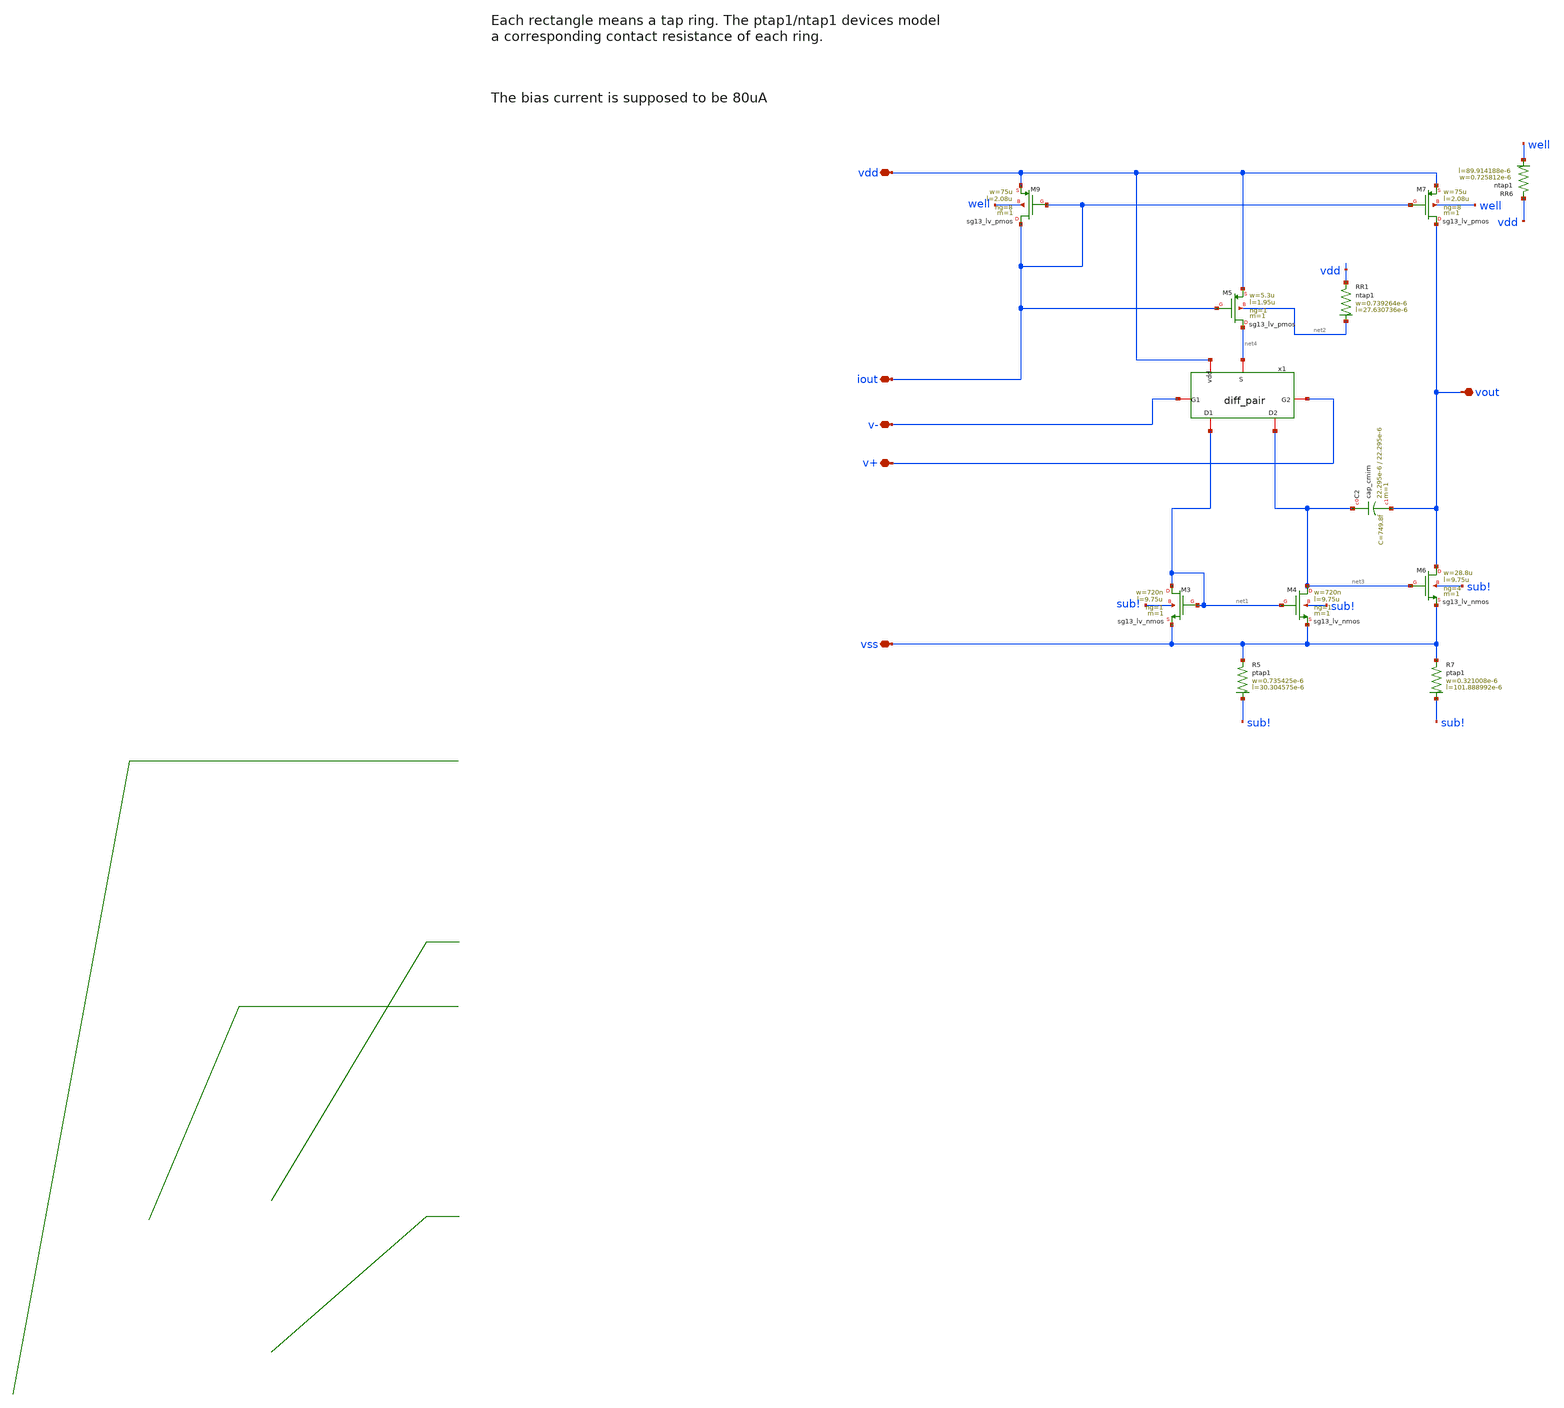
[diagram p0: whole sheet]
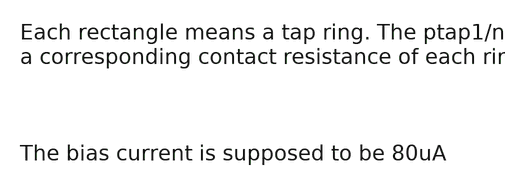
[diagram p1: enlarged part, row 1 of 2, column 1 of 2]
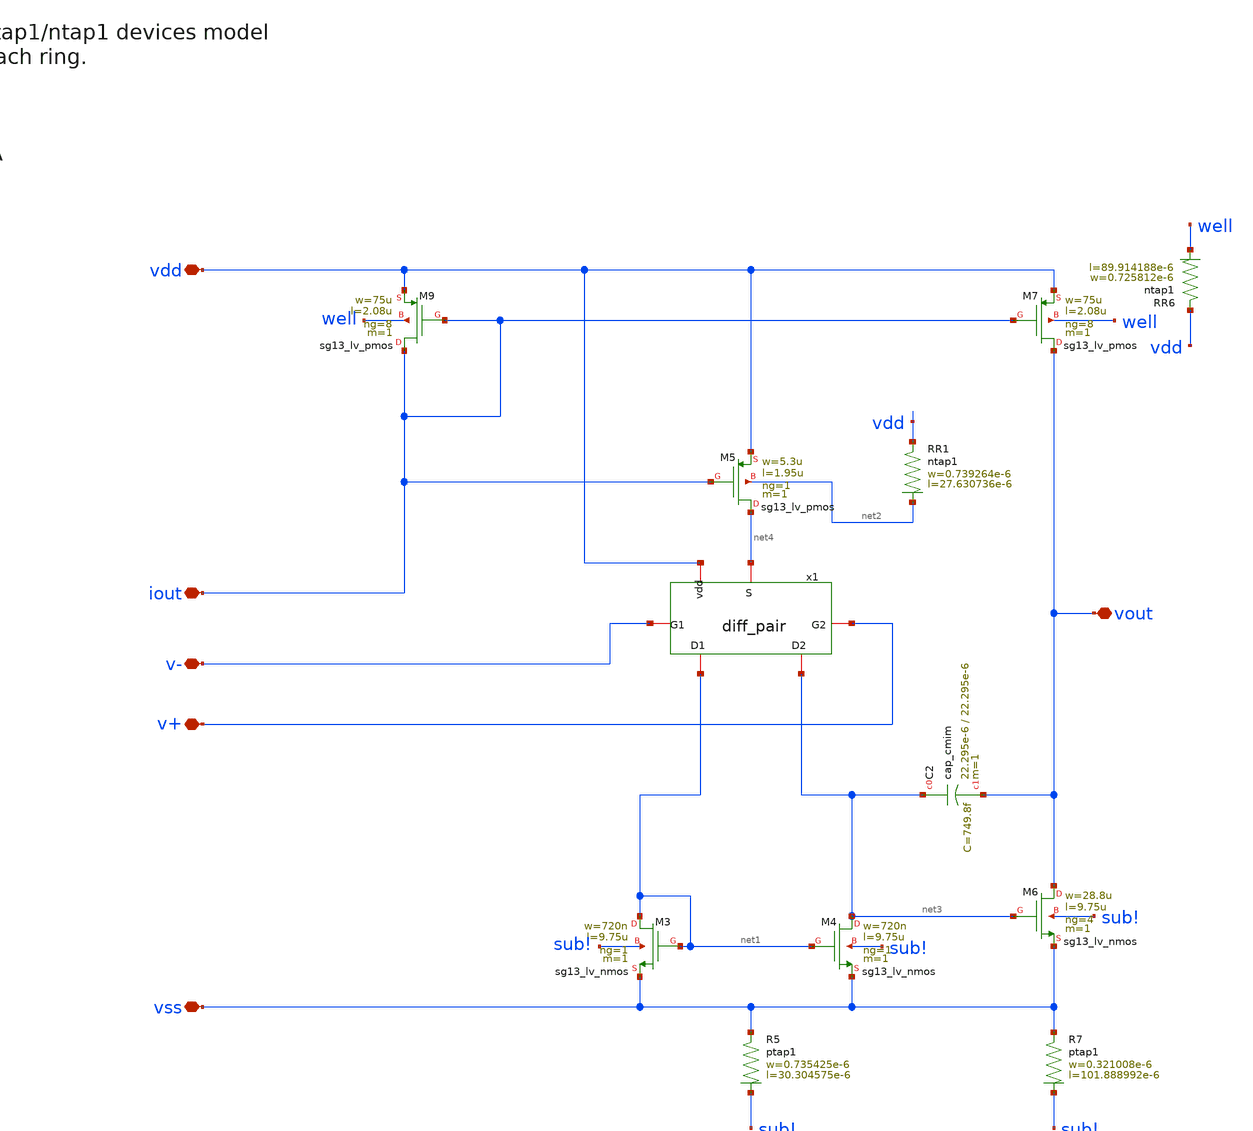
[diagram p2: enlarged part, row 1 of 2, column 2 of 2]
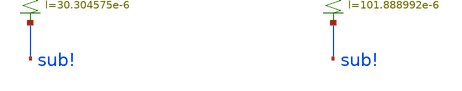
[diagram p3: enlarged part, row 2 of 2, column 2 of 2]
** sch_path: tests/data/_corecheck/from-final-core/OTA1336-final.sch
**.subckt OTA1336-final v- v+ vss vdd iout vout
*.iopin v-
*.iopin v+
*.iopin vss
*.iopin vdd
*.iopin iout
*.iopin vout
XM4 net3 net1 vss sub! sg13_lv_nmos w=720n l=9.75u ng=1 m=1 mm_ok=0
XM3 net1 net1 vss sub! sg13_lv_nmos w=720n l=9.75u ng=1 m=1 mm_ok=0
XM5 net4 iout vdd net2 sg13_lv_pmos w=5.3u l=1.95u ng=1 m=1 mm_ok=0
XM7 vout iout vdd well sg13_lv_pmos w=75u l=2.08u ng=8 m=1 mm_ok=0
XM6 vout net3 vss sub! sg13_lv_nmos w=28.8u l=9.75u ng=4 m=1 mm_ok=0
XM9 iout iout vdd well sg13_lv_pmos w=75u l=2.08u ng=8 m=1 mm_ok=0
XC2 net3 vout cap_cmim w=22.295e-6 l=22.295e-6 m=1 mm_ok=1
XR6 vdd well ntap1 R=3.975 w=0.725812e-6 l=89.914188e-6
XR5 vss sub! ptap1 R=11.62 w=0.735425e-6 l=30.304575e-6
XR7 vss sub! ptap1 R=4.133 w=0.321008e-6 l=101.888992e-6
XR1 vdd net2 ntap1 R=12.7 w=0.739264e-6 l=27.630736e-6
x1 vdd net4 v- v+ net1 net3 diff_pair
**.ends

* expanding   symbol:  diff_pair.sym # of pins=6
** sym_path: tests/data/OTA1336/schematic/xschem/diff_pair.sym
** sch_path: tests/data/OTA1336/schematic/xschem/diff_pair.sch
.subckt diff_pair vdd S G1 G2 D1 D2
*.iopin D1
*.iopin D2
*.iopin vdd
*.iopin S
*.iopin G1
*.iopin G2
XM1 D2 G2 S b sg13_lv_pmos w=3.64u l=3.7u ng=1 m=1 mm_ok=0
XM13 vdd vdd S b sg13_lv_pmos w=3.64u l=3.7u ng=1 m=1 mm_ok=0
XR1 vdd b ntap1 R=4.518 w=0.3614421e-6 l=91.558579e-6
XM8 D2 vdd vdd b sg13_lv_pmos w=3.64u l=3.7u ng=1 m=1 mm_ok=0
XM2 D1 G1 S b sg13_lv_pmos w=3.64u l=3.7u ng=1 m=1 mm_ok=0
XM3 vdd vdd S b sg13_lv_pmos w=3.64u l=3.7u ng=1 m=1 mm_ok=0
XM4 D1 vdd vdd b sg13_lv_pmos w=3.64u l=3.7u ng=1 m=1 mm_ok=0
XM5 D1 G1 S b sg13_lv_pmos w=3.64u l=3.7u ng=1 m=1 mm_ok=0
XM6 vdd vdd S b sg13_lv_pmos w=3.64u l=3.7u ng=1 m=1 mm_ok=0
XM7 D1 vdd vdd b sg13_lv_pmos w=3.64u l=3.7u ng=1 m=1 mm_ok=0
XM9 D2 G2 S b sg13_lv_pmos w=3.64u l=3.7u ng=1 m=1 mm_ok=0
XM10 vdd vdd S b sg13_lv_pmos w=3.64u l=3.7u ng=1 m=1 mm_ok=0
XM11 D2 vdd vdd b sg13_lv_pmos w=3.64u l=3.7u ng=1 m=1 mm_ok=0
.ends

.end
